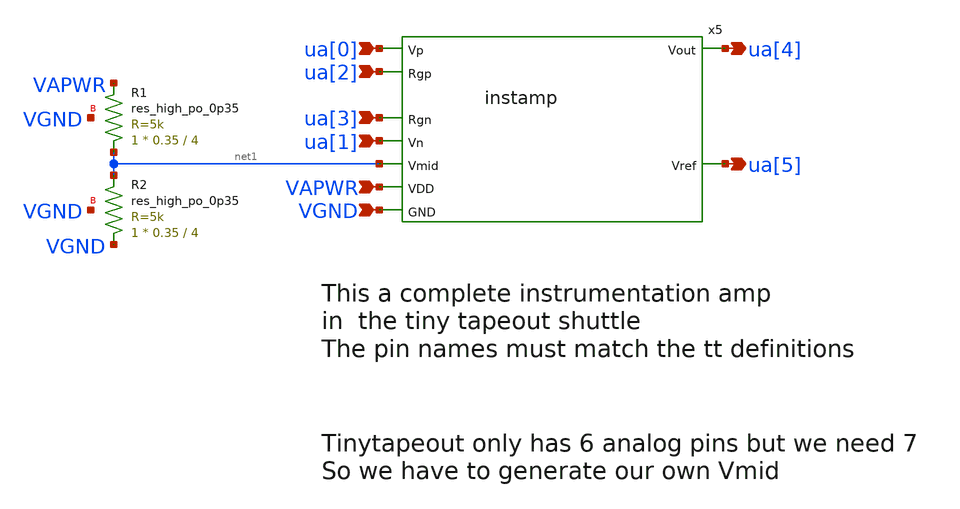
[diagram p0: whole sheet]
** sch_path: xschem/tt_um_jonathanwest3_instamp_sp2026.sch
* Copyright 2021 Stefan Frederik Schippers
* Licensed under the Apache License, Version 2.0 (the "License");
* you may not use this file except in compliance with the License.
* You may obtain a copy of the License at
* https://www.apache.org/licenses/LICENSE-2.0
* Unless required by applicable law or agreed to in writing, software
* distributed under the License is distributed on an "AS IS" BASIS,
* WITHOUT WARRANTIES OR CONDITIONS OF ANY KIND, either express or implied.
* See the License for the specific language governing permissions and
* limitations under the License.
**.subckt tt_um_jonathanwest3_instamp_sp2026 ua[0] ua[1] ua[4] ua[5] ua[2] ua[3] VGND VAPWR
*.ipin ua[0]
*.ipin ua[1]
*.opin ua[4]
*.opin ua[5]
*.ipin ua[2]
*.ipin ua[3]
*.ipin VGND
*.ipin VAPWR
x5 ua[1] ua[3] ua[0] ua[2] net1 ua[4] ua[5] VAPWR VGND instamp
XR1 net1 VAPWR VGND sky130_fd_pr__res_high_po_0p35 L=4 mult=1 m=1
XR2 VGND net1 VGND sky130_fd_pr__res_high_po_0p35 L=4 mult=1 m=1
**.ends
.end
